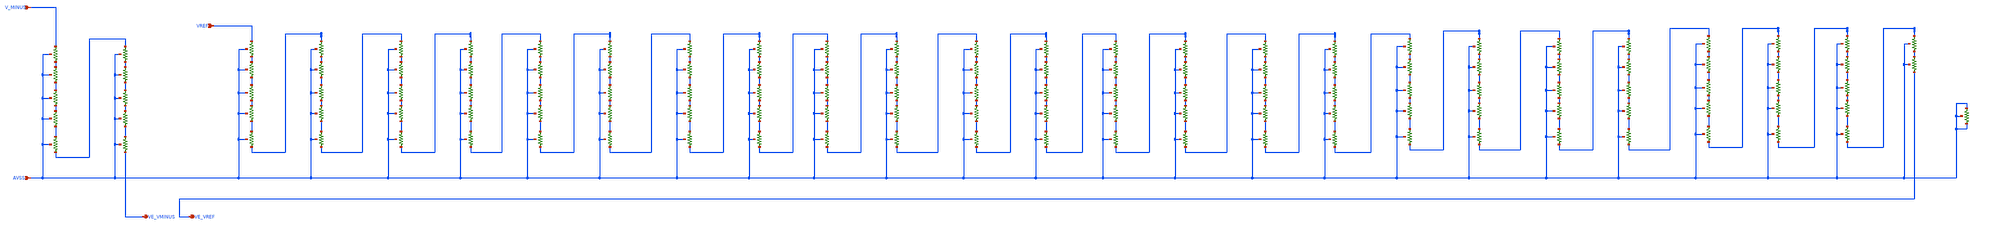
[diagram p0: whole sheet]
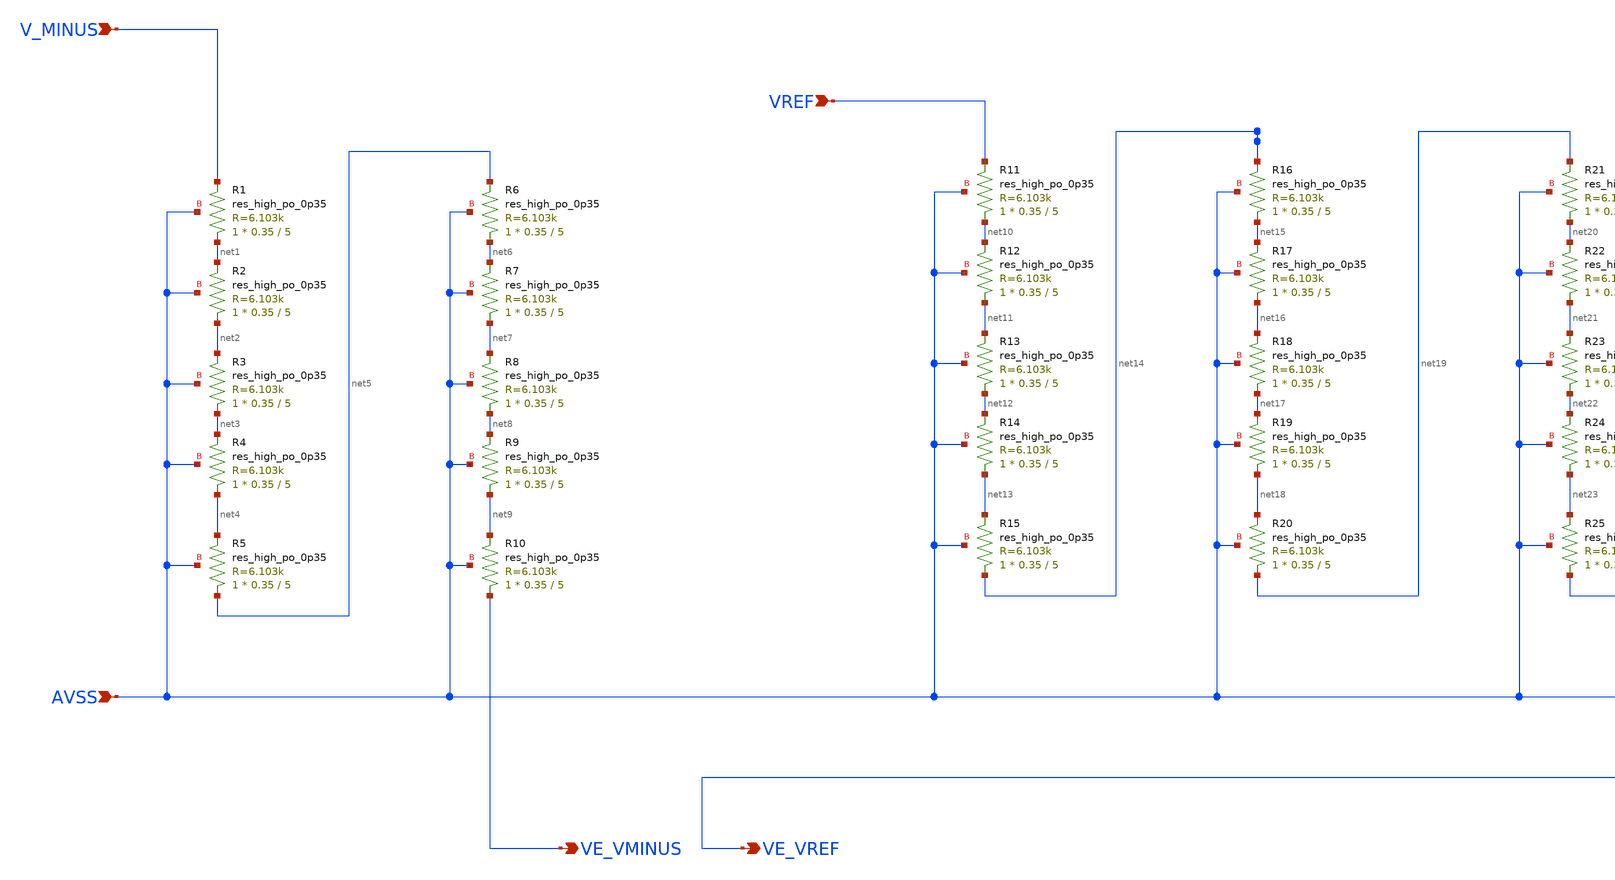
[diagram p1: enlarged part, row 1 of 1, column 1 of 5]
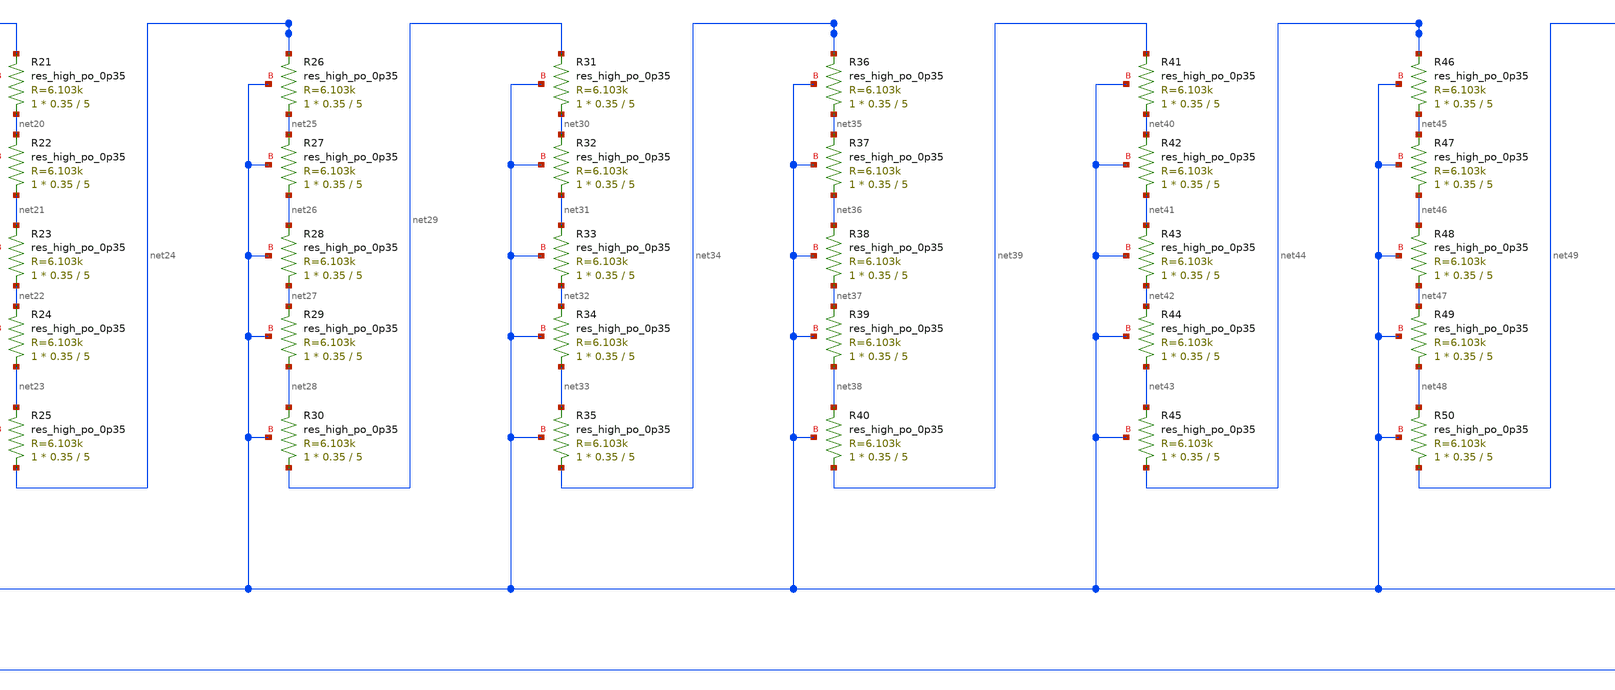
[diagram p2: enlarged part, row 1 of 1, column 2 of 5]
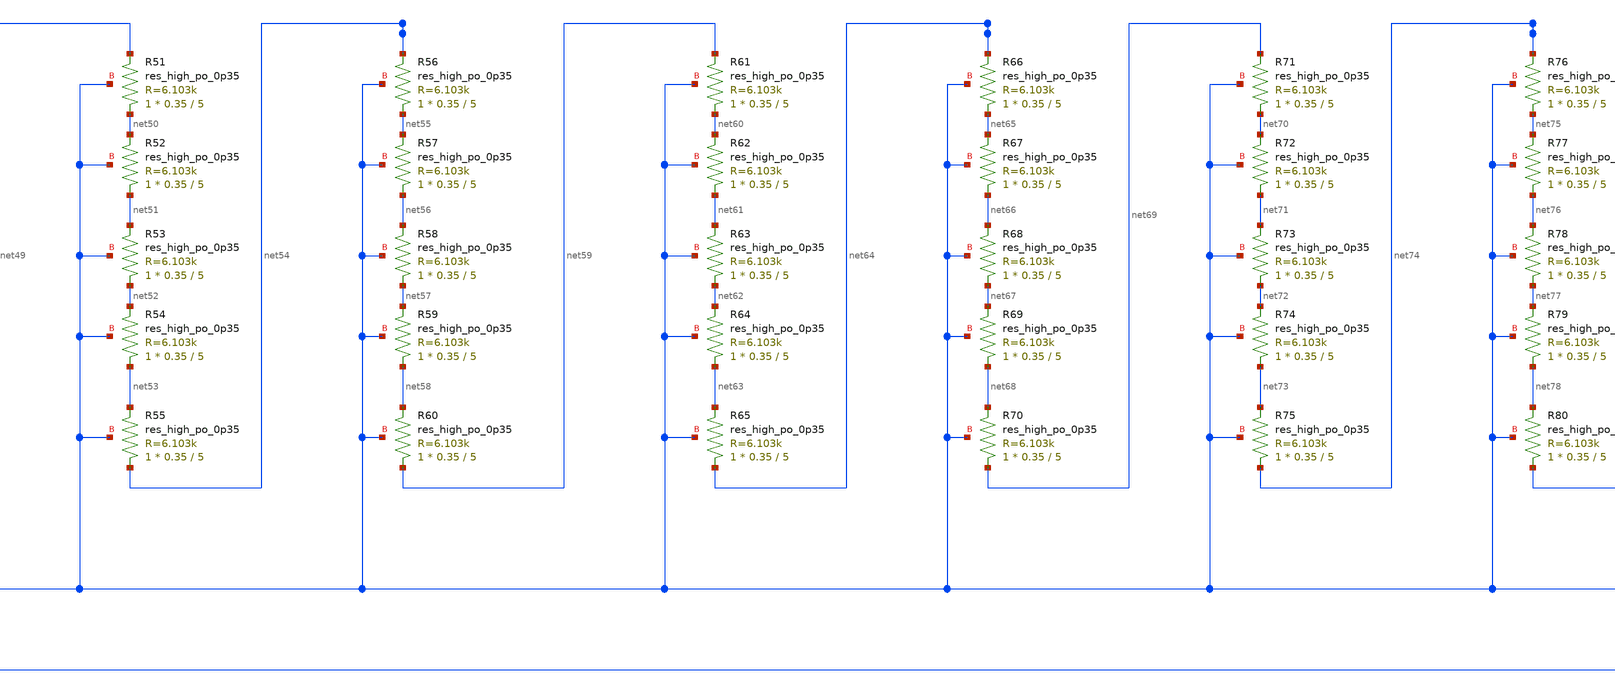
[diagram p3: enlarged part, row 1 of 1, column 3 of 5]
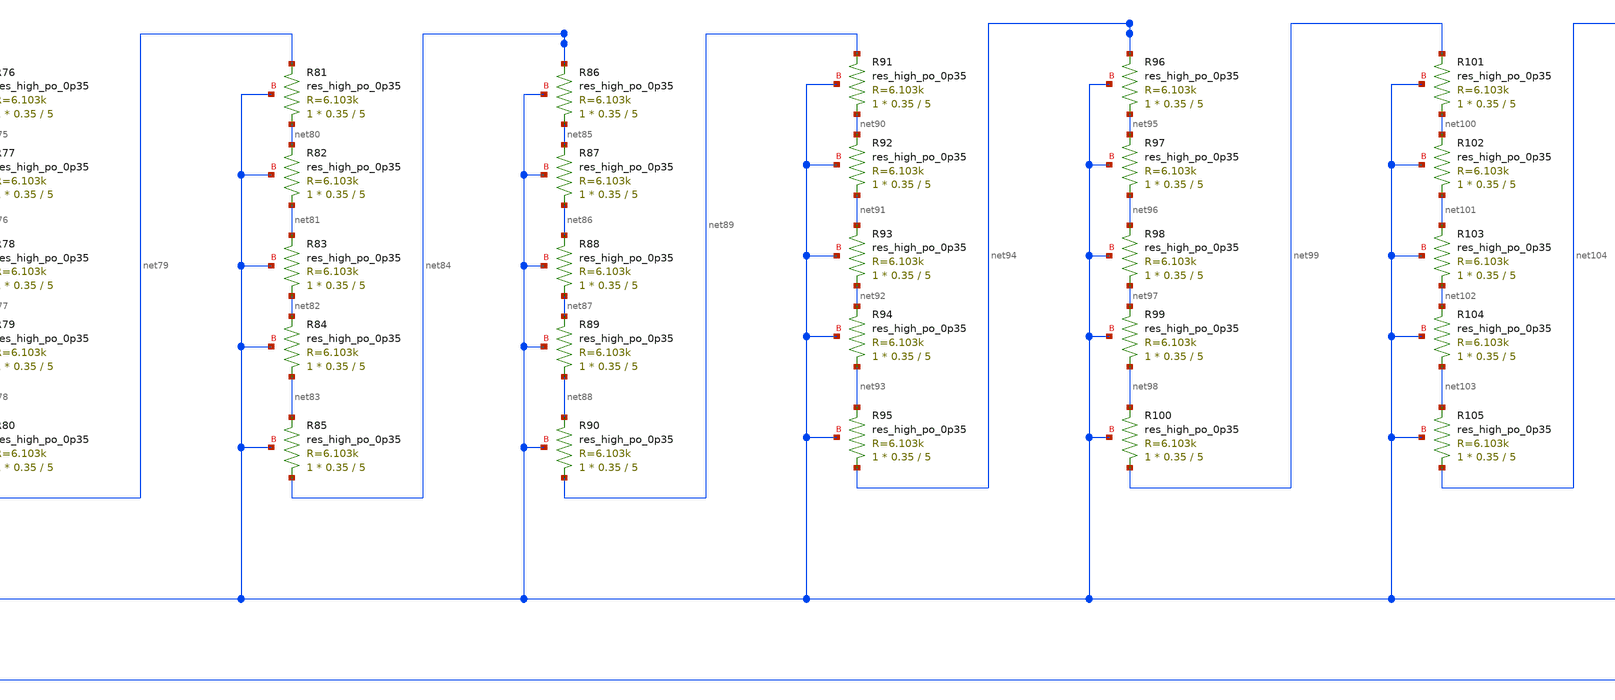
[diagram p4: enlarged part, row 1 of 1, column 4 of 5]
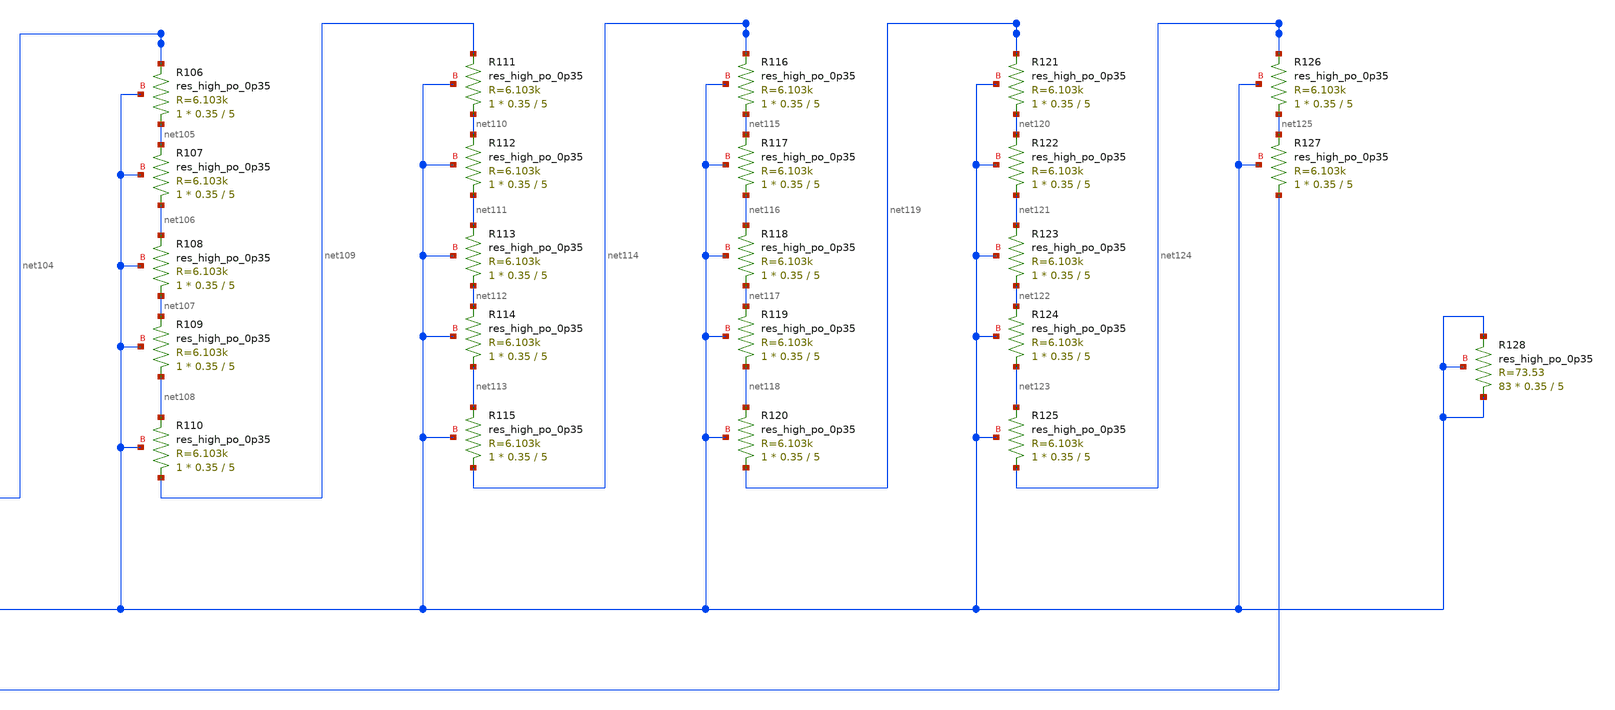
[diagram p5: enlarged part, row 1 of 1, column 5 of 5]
** sch_path: lef/bg2_res_array_complete.sch
**.subckt bg2_res_array_complete V_MINUS VE_VMINUS AVSS VREF VE_VREF
*.ipin V_MINUS
*.opin VE_VMINUS
*.ipin AVSS
*.ipin VREF
*.opin VE_VREF
XR1 net1 V_MINUS AVSS sky130_fd_pr__res_high_po_0p35 L=5 mult=1 m=1
XR2 net2 net1 AVSS sky130_fd_pr__res_high_po_0p35 L=5 mult=1 m=1
XR3 net3 net2 AVSS sky130_fd_pr__res_high_po_0p35 L=5 mult=1 m=1
XR4 net4 net3 AVSS sky130_fd_pr__res_high_po_0p35 L=5 mult=1 m=1
XR5 net5 net4 AVSS sky130_fd_pr__res_high_po_0p35 L=5 mult=1 m=1
XR6 net6 net5 AVSS sky130_fd_pr__res_high_po_0p35 L=5 mult=1 m=1
XR7 net7 net6 AVSS sky130_fd_pr__res_high_po_0p35 L=5 mult=1 m=1
XR8 net8 net7 AVSS sky130_fd_pr__res_high_po_0p35 L=5 mult=1 m=1
XR9 net9 net8 AVSS sky130_fd_pr__res_high_po_0p35 L=5 mult=1 m=1
XR10 VE_VMINUS net9 AVSS sky130_fd_pr__res_high_po_0p35 L=5 mult=1 m=1
XR11 net10 VREF AVSS sky130_fd_pr__res_high_po_0p35 L=5 mult=1 m=1
XR12 net11 net10 AVSS sky130_fd_pr__res_high_po_0p35 L=5 mult=1 m=1
XR13 net12 net11 AVSS sky130_fd_pr__res_high_po_0p35 L=5 mult=1 m=1
XR14 net13 net12 AVSS sky130_fd_pr__res_high_po_0p35 L=5 mult=1 m=1
XR15 net14 net13 AVSS sky130_fd_pr__res_high_po_0p35 L=5 mult=1 m=1
XR16 net15 net14 AVSS sky130_fd_pr__res_high_po_0p35 L=5 mult=1 m=1
XR17 net16 net15 AVSS sky130_fd_pr__res_high_po_0p35 L=5 mult=1 m=1
XR18 net17 net16 AVSS sky130_fd_pr__res_high_po_0p35 L=5 mult=1 m=1
XR19 net18 net17 AVSS sky130_fd_pr__res_high_po_0p35 L=5 mult=1 m=1
XR20 net19 net18 AVSS sky130_fd_pr__res_high_po_0p35 L=5 mult=1 m=1
XR21 net20 net19 AVSS sky130_fd_pr__res_high_po_0p35 L=5 mult=1 m=1
XR22 net21 net20 AVSS sky130_fd_pr__res_high_po_0p35 L=5 mult=1 m=1
XR23 net22 net21 AVSS sky130_fd_pr__res_high_po_0p35 L=5 mult=1 m=1
XR24 net23 net22 AVSS sky130_fd_pr__res_high_po_0p35 L=5 mult=1 m=1
XR25 net24 net23 AVSS sky130_fd_pr__res_high_po_0p35 L=5 mult=1 m=1
XR26 net25 net24 AVSS sky130_fd_pr__res_high_po_0p35 L=5 mult=1 m=1
XR27 net26 net25 AVSS sky130_fd_pr__res_high_po_0p35 L=5 mult=1 m=1
XR28 net27 net26 AVSS sky130_fd_pr__res_high_po_0p35 L=5 mult=1 m=1
XR29 net28 net27 AVSS sky130_fd_pr__res_high_po_0p35 L=5 mult=1 m=1
XR30 net29 net28 AVSS sky130_fd_pr__res_high_po_0p35 L=5 mult=1 m=1
XR31 net30 net29 AVSS sky130_fd_pr__res_high_po_0p35 L=5 mult=1 m=1
XR32 net31 net30 AVSS sky130_fd_pr__res_high_po_0p35 L=5 mult=1 m=1
XR33 net32 net31 AVSS sky130_fd_pr__res_high_po_0p35 L=5 mult=1 m=1
XR34 net33 net32 AVSS sky130_fd_pr__res_high_po_0p35 L=5 mult=1 m=1
XR35 net34 net33 AVSS sky130_fd_pr__res_high_po_0p35 L=5 mult=1 m=1
XR36 net35 net34 AVSS sky130_fd_pr__res_high_po_0p35 L=5 mult=1 m=1
XR37 net36 net35 AVSS sky130_fd_pr__res_high_po_0p35 L=5 mult=1 m=1
XR38 net37 net36 AVSS sky130_fd_pr__res_high_po_0p35 L=5 mult=1 m=1
XR39 net38 net37 AVSS sky130_fd_pr__res_high_po_0p35 L=5 mult=1 m=1
XR40 net39 net38 AVSS sky130_fd_pr__res_high_po_0p35 L=5 mult=1 m=1
XR41 net40 net39 AVSS sky130_fd_pr__res_high_po_0p35 L=5 mult=1 m=1
XR42 net41 net40 AVSS sky130_fd_pr__res_high_po_0p35 L=5 mult=1 m=1
XR43 net42 net41 AVSS sky130_fd_pr__res_high_po_0p35 L=5 mult=1 m=1
XR44 net43 net42 AVSS sky130_fd_pr__res_high_po_0p35 L=5 mult=1 m=1
XR45 net44 net43 AVSS sky130_fd_pr__res_high_po_0p35 L=5 mult=1 m=1
XR46 net45 net44 AVSS sky130_fd_pr__res_high_po_0p35 L=5 mult=1 m=1
XR47 net46 net45 AVSS sky130_fd_pr__res_high_po_0p35 L=5 mult=1 m=1
XR48 net47 net46 AVSS sky130_fd_pr__res_high_po_0p35 L=5 mult=1 m=1
XR49 net48 net47 AVSS sky130_fd_pr__res_high_po_0p35 L=5 mult=1 m=1
XR50 net49 net48 AVSS sky130_fd_pr__res_high_po_0p35 L=5 mult=1 m=1
XR51 net50 net49 AVSS sky130_fd_pr__res_high_po_0p35 L=5 mult=1 m=1
XR52 net51 net50 AVSS sky130_fd_pr__res_high_po_0p35 L=5 mult=1 m=1
XR53 net52 net51 AVSS sky130_fd_pr__res_high_po_0p35 L=5 mult=1 m=1
XR54 net53 net52 AVSS sky130_fd_pr__res_high_po_0p35 L=5 mult=1 m=1
XR55 net54 net53 AVSS sky130_fd_pr__res_high_po_0p35 L=5 mult=1 m=1
XR56 net55 net54 AVSS sky130_fd_pr__res_high_po_0p35 L=5 mult=1 m=1
XR57 net56 net55 AVSS sky130_fd_pr__res_high_po_0p35 L=5 mult=1 m=1
XR58 net57 net56 AVSS sky130_fd_pr__res_high_po_0p35 L=5 mult=1 m=1
XR59 net58 net57 AVSS sky130_fd_pr__res_high_po_0p35 L=5 mult=1 m=1
XR60 net59 net58 AVSS sky130_fd_pr__res_high_po_0p35 L=5 mult=1 m=1
XR61 net60 net59 AVSS sky130_fd_pr__res_high_po_0p35 L=5 mult=1 m=1
XR62 net61 net60 AVSS sky130_fd_pr__res_high_po_0p35 L=5 mult=1 m=1
XR63 net62 net61 AVSS sky130_fd_pr__res_high_po_0p35 L=5 mult=1 m=1
XR64 net63 net62 AVSS sky130_fd_pr__res_high_po_0p35 L=5 mult=1 m=1
XR65 net64 net63 AVSS sky130_fd_pr__res_high_po_0p35 L=5 mult=1 m=1
XR66 net65 net64 AVSS sky130_fd_pr__res_high_po_0p35 L=5 mult=1 m=1
XR67 net66 net65 AVSS sky130_fd_pr__res_high_po_0p35 L=5 mult=1 m=1
XR68 net67 net66 AVSS sky130_fd_pr__res_high_po_0p35 L=5 mult=1 m=1
XR69 net68 net67 AVSS sky130_fd_pr__res_high_po_0p35 L=5 mult=1 m=1
XR70 net69 net68 AVSS sky130_fd_pr__res_high_po_0p35 L=5 mult=1 m=1
XR71 net70 net69 AVSS sky130_fd_pr__res_high_po_0p35 L=5 mult=1 m=1
XR72 net71 net70 AVSS sky130_fd_pr__res_high_po_0p35 L=5 mult=1 m=1
XR73 net72 net71 AVSS sky130_fd_pr__res_high_po_0p35 L=5 mult=1 m=1
XR74 net73 net72 AVSS sky130_fd_pr__res_high_po_0p35 L=5 mult=1 m=1
XR75 net74 net73 AVSS sky130_fd_pr__res_high_po_0p35 L=5 mult=1 m=1
XR76 net75 net74 AVSS sky130_fd_pr__res_high_po_0p35 L=5 mult=1 m=1
XR77 net76 net75 AVSS sky130_fd_pr__res_high_po_0p35 L=5 mult=1 m=1
XR78 net77 net76 AVSS sky130_fd_pr__res_high_po_0p35 L=5 mult=1 m=1
XR79 net78 net77 AVSS sky130_fd_pr__res_high_po_0p35 L=5 mult=1 m=1
XR80 net79 net78 AVSS sky130_fd_pr__res_high_po_0p35 L=5 mult=1 m=1
XR81 net80 net79 AVSS sky130_fd_pr__res_high_po_0p35 L=5 mult=1 m=1
XR82 net81 net80 AVSS sky130_fd_pr__res_high_po_0p35 L=5 mult=1 m=1
XR83 net82 net81 AVSS sky130_fd_pr__res_high_po_0p35 L=5 mult=1 m=1
XR84 net83 net82 AVSS sky130_fd_pr__res_high_po_0p35 L=5 mult=1 m=1
XR85 net84 net83 AVSS sky130_fd_pr__res_high_po_0p35 L=5 mult=1 m=1
XR86 net85 net84 AVSS sky130_fd_pr__res_high_po_0p35 L=5 mult=1 m=1
XR87 net86 net85 AVSS sky130_fd_pr__res_high_po_0p35 L=5 mult=1 m=1
XR88 net87 net86 AVSS sky130_fd_pr__res_high_po_0p35 L=5 mult=1 m=1
XR89 net88 net87 AVSS sky130_fd_pr__res_high_po_0p35 L=5 mult=1 m=1
XR90 net89 net88 AVSS sky130_fd_pr__res_high_po_0p35 L=5 mult=1 m=1
XR91 net90 net89 AVSS sky130_fd_pr__res_high_po_0p35 L=5 mult=1 m=1
XR92 net91 net90 AVSS sky130_fd_pr__res_high_po_0p35 L=5 mult=1 m=1
XR93 net92 net91 AVSS sky130_fd_pr__res_high_po_0p35 L=5 mult=1 m=1
XR94 net93 net92 AVSS sky130_fd_pr__res_high_po_0p35 L=5 mult=1 m=1
XR95 net94 net93 AVSS sky130_fd_pr__res_high_po_0p35 L=5 mult=1 m=1
XR96 net95 net94 AVSS sky130_fd_pr__res_high_po_0p35 L=5 mult=1 m=1
XR97 net96 net95 AVSS sky130_fd_pr__res_high_po_0p35 L=5 mult=1 m=1
XR98 net97 net96 AVSS sky130_fd_pr__res_high_po_0p35 L=5 mult=1 m=1
XR99 net98 net97 AVSS sky130_fd_pr__res_high_po_0p35 L=5 mult=1 m=1
XR100 net99 net98 AVSS sky130_fd_pr__res_high_po_0p35 L=5 mult=1 m=1
XR101 net100 net99 AVSS sky130_fd_pr__res_high_po_0p35 L=5 mult=1 m=1
XR102 net101 net100 AVSS sky130_fd_pr__res_high_po_0p35 L=5 mult=1 m=1
XR103 net102 net101 AVSS sky130_fd_pr__res_high_po_0p35 L=5 mult=1 m=1
XR104 net103 net102 AVSS sky130_fd_pr__res_high_po_0p35 L=5 mult=1 m=1
XR105 net104 net103 AVSS sky130_fd_pr__res_high_po_0p35 L=5 mult=1 m=1
XR106 net105 net104 AVSS sky130_fd_pr__res_high_po_0p35 L=5 mult=1 m=1
XR107 net106 net105 AVSS sky130_fd_pr__res_high_po_0p35 L=5 mult=1 m=1
XR108 net107 net106 AVSS sky130_fd_pr__res_high_po_0p35 L=5 mult=1 m=1
XR109 net108 net107 AVSS sky130_fd_pr__res_high_po_0p35 L=5 mult=1 m=1
XR110 net109 net108 AVSS sky130_fd_pr__res_high_po_0p35 L=5 mult=1 m=1
XR111 net110 net109 AVSS sky130_fd_pr__res_high_po_0p35 L=5 mult=1 m=1
XR112 net111 net110 AVSS sky130_fd_pr__res_high_po_0p35 L=5 mult=1 m=1
XR113 net112 net111 AVSS sky130_fd_pr__res_high_po_0p35 L=5 mult=1 m=1
XR114 net113 net112 AVSS sky130_fd_pr__res_high_po_0p35 L=5 mult=1 m=1
XR115 net114 net113 AVSS sky130_fd_pr__res_high_po_0p35 L=5 mult=1 m=1
XR116 net115 net114 AVSS sky130_fd_pr__res_high_po_0p35 L=5 mult=1 m=1
XR117 net116 net115 AVSS sky130_fd_pr__res_high_po_0p35 L=5 mult=1 m=1
XR118 net117 net116 AVSS sky130_fd_pr__res_high_po_0p35 L=5 mult=1 m=1
XR119 net118 net117 AVSS sky130_fd_pr__res_high_po_0p35 L=5 mult=1 m=1
XR120 net119 net118 AVSS sky130_fd_pr__res_high_po_0p35 L=5 mult=1 m=1
XR121 net120 net119 AVSS sky130_fd_pr__res_high_po_0p35 L=5 mult=1 m=1
XR122 net121 net120 AVSS sky130_fd_pr__res_high_po_0p35 L=5 mult=1 m=1
XR123 net122 net121 AVSS sky130_fd_pr__res_high_po_0p35 L=5 mult=1 m=1
XR124 net123 net122 AVSS sky130_fd_pr__res_high_po_0p35 L=5 mult=1 m=1
XR125 net124 net123 AVSS sky130_fd_pr__res_high_po_0p35 L=5 mult=1 m=1
XR126 net125 net124 AVSS sky130_fd_pr__res_high_po_0p35 L=5 mult=1 m=1
XR127 VE_VREF net125 AVSS sky130_fd_pr__res_high_po_0p35 L=5 mult=1 m=1
XR128 AVSS AVSS AVSS sky130_fd_pr__res_high_po_0p35 L=5 mult=83 m=83
**.ends
.end
